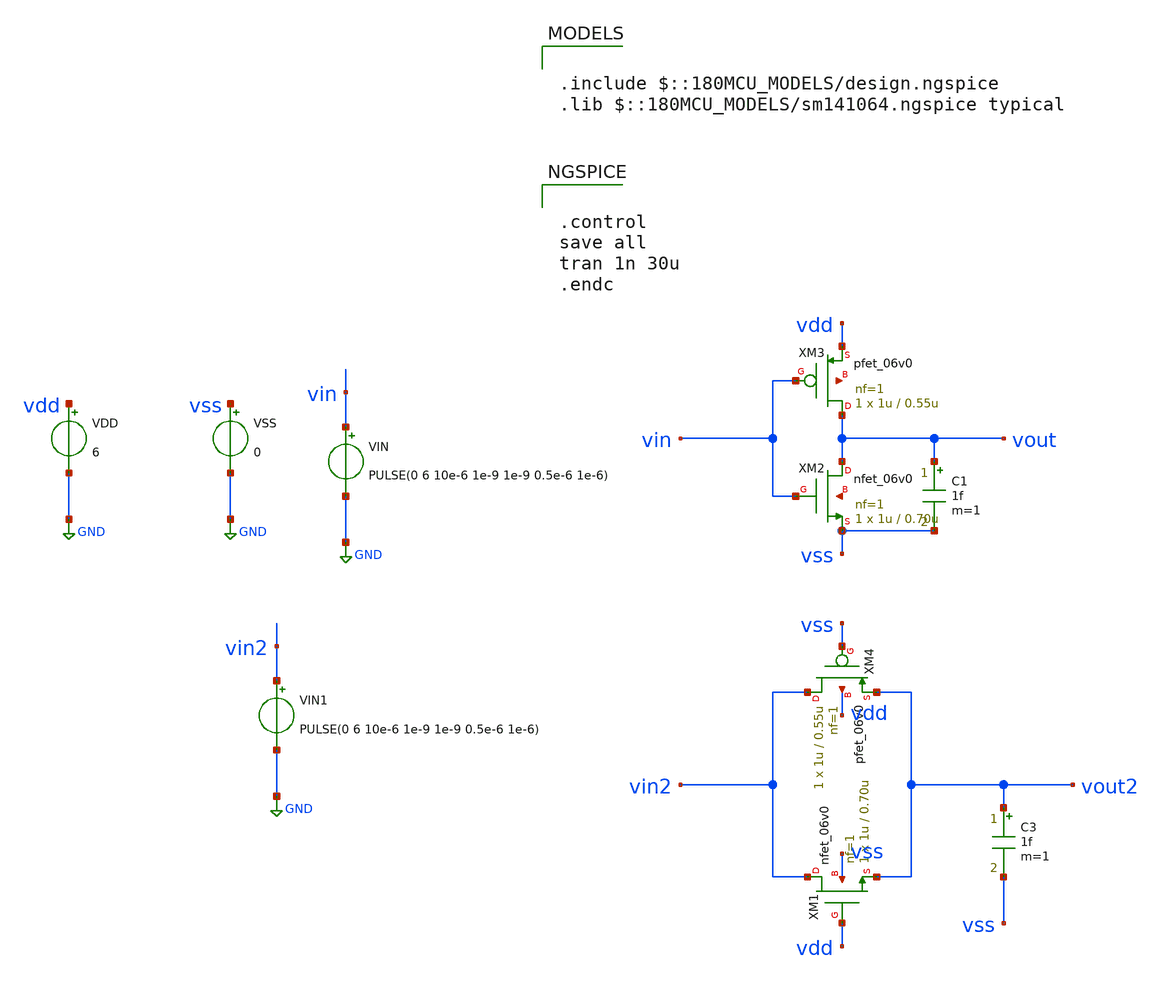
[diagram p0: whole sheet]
** sch_path: xschem/gf_test/inv_tyoketu.sch
**.subckt inv_tyoketu
XM2 vout vin vss net1 nfet_06v0 L=0.70u W=1u nf=1 ad='int((nf+1)/2) * W/nf * 0.18u' as='int((nf+2)/2) * W/nf * 0.18u'
+ pd='2*int((nf+1)/2) * (W/nf + 0.18u)' ps='2*int((nf+2)/2) * (W/nf + 0.18u)' nrd='0.18u / W' nrs='0.18u / W'
+ sa=0 sb=0 sd=0 m=1
XM3 vout vin vdd net2 pfet_06v0 L=0.55u W=1u nf=1 ad='int((nf+1)/2) * W/nf * 0.18u' as='int((nf+2)/2) * W/nf * 0.18u'
+ pd='2*int((nf+1)/2) * (W/nf + 0.18u)' ps='2*int((nf+2)/2) * (W/nf + 0.18u)' nrd='0.18u / W' nrs='0.18u / W'
+ sa=0 sb=0 sd=0 m=1
C1 vout vss 1f m=1
VSS vss GND 0
VDD vdd GND 6
VIN vin GND PULSE(0 6 10e-6 1e-9 1e-9 0.5e-6 1e-6)
XM1 vin2 vdd vout2 vss nfet_06v0 L=0.70u W=1u nf=1 ad='int((nf+1)/2) * W/nf * 0.18u' as='int((nf+2)/2) * W/nf * 0.18u'
+ pd='2*int((nf+1)/2) * (W/nf + 0.18u)' ps='2*int((nf+2)/2) * (W/nf + 0.18u)' nrd='0.18u / W' nrs='0.18u / W'
+ sa=0 sb=0 sd=0 m=1
XM4 vin2 vss vout2 vdd pfet_06v0 L=0.55u W=1u nf=1 ad='int((nf+1)/2) * W/nf * 0.18u' as='int((nf+2)/2) * W/nf * 0.18u'
+ pd='2*int((nf+1)/2) * (W/nf + 0.18u)' ps='2*int((nf+2)/2) * (W/nf + 0.18u)' nrd='0.18u / W' nrs='0.18u / W'
+ sa=0 sb=0 sd=0 m=1
C3 vout2 vss 1f m=1
VIN1 vin2 GND PULSE(0 6 10e-6 1e-9 1e-9 0.5e-6 1e-6)
**** begin user architecture code

.include $::180MCU_MODELS/design.ngspice
.lib $::180MCU_MODELS/sm141064.ngspice typical



.control
save all
tran 1n 30u
.endc


**** end user architecture code
**.ends
.GLOBAL GND
.end
